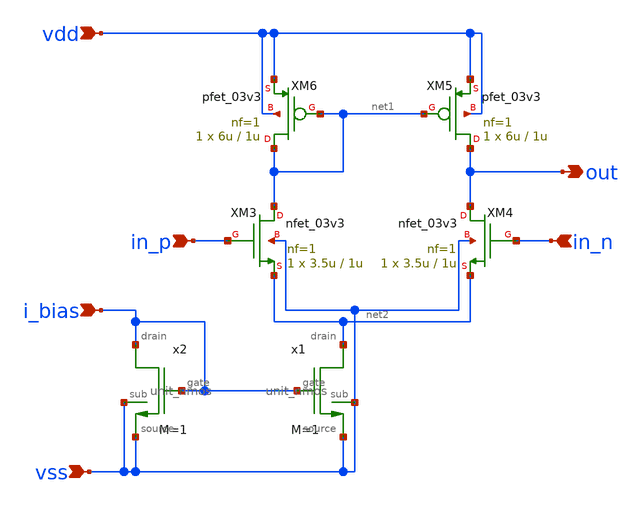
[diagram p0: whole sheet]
** sch_path: designs/libs/core_analog/ota_5t/ota_5t.sch
**.subckt ota_5t in_p in_n i_bias vdd vss out
*.ipin in_p
*.ipin in_n
*.ipin i_bias
*.ipin vdd
*.ipin vss
*.opin out
XM3 net1 in_p net2 vss nfet_03v3 L=1u W=3.5u nf=1 ad='int((nf+1)/2) * W/nf * 0.18u' as='int((nf+2)/2) * W/nf * 0.18u'
+ pd='2*int((nf+1)/2) * (W/nf + 0.18u)' ps='2*int((nf+2)/2) * (W/nf + 0.18u)' nrd='0.18u / W' nrs='0.18u / W'
+ sa=0 sb=0 sd=0 m=1
XM4 out in_n net2 vss nfet_03v3 L=1u W=3.5u nf=1 ad='int((nf+1)/2) * W/nf * 0.18u' as='int((nf+2)/2) * W/nf * 0.18u'
+ pd='2*int((nf+1)/2) * (W/nf + 0.18u)' ps='2*int((nf+2)/2) * (W/nf + 0.18u)' nrd='0.18u / W' nrs='0.18u / W'
+ sa=0 sb=0 sd=0 m=1
XM5 out net1 vdd vdd pfet_03v3 L=1u W=6u nf=1 ad='int((nf+1)/2) * W/nf * 0.18u' as='int((nf+2)/2) * W/nf * 0.18u'
+ pd='2*int((nf+1)/2) * (W/nf + 0.18u)' ps='2*int((nf+2)/2) * (W/nf + 0.18u)' nrd='0.18u / W' nrs='0.18u / W'
+ sa=0 sb=0 sd=0 m=1
XM6 net1 net1 vdd vdd pfet_03v3 L=1u W=6u nf=1 ad='int((nf+1)/2) * W/nf * 0.18u' as='int((nf+2)/2) * W/nf * 0.18u'
+ pd='2*int((nf+1)/2) * (W/nf + 0.18u)' ps='2*int((nf+2)/2) * (W/nf + 0.18u)' nrd='0.18u / W' nrs='0.18u / W'
+ sa=0 sb=0 sd=0 m=1
x1 net2 vss i_bias vss unit_nmos M=1
x2 i_bias vss i_bias vss unit_nmos M=1
**.ends

* expanding   symbol:  libs/core_analog/unit_nmos/unit_nmos.sym # of pins=4
** sym_path: libs/core_analog/unit_nmos/unit_nmos.sym
** sch_path: libs/core_analog/unit_nmos/unit_nmos.sch
.subckt unit_nmos drain sub gate source
*.iopin drain
*.iopin source
*.iopin sub
*.iopin gate
XM1 drain gate source sub nfet_03v3 L=1u W=2.5u nf=1 ad='int((nf+1)/2) * W/nf * 0.18u' as='int((nf+2)/2) * W/nf * 0.18u'
+ pd='2*int((nf+1)/2) * (W/nf + 0.18u)' ps='2*int((nf+2)/2) * (W/nf + 0.18u)' nrd='0.18u / W' nrs='0.18u / W'
+ sa=0 sb=0 sd=0 m={M}
**** begin user architecture code

.param M=1

**** end user architecture code
.ends

.end
